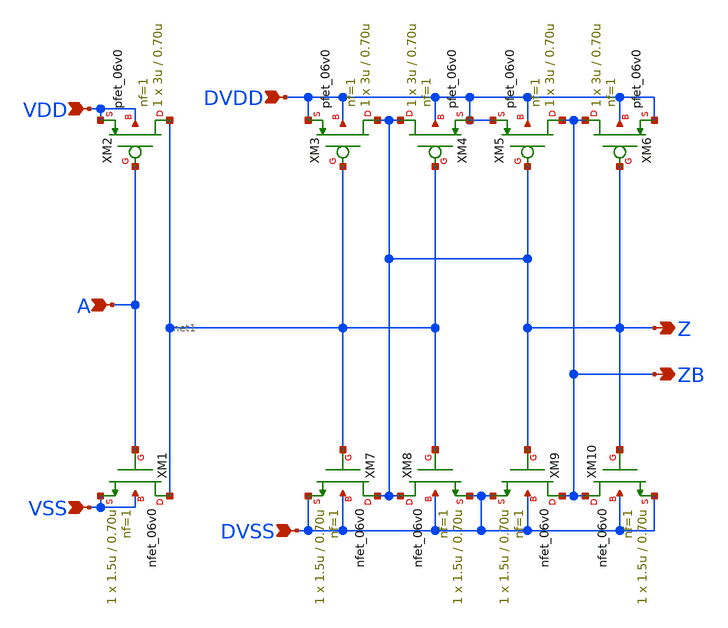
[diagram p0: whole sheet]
** sch_path: gf180mcu_fd_io__bi_24t/comp018green_sigbuf_1.sch
**.subckt comp018green_sigbuf_1 A VDD VSS DVDD DVSS Z ZB
*.ipin A
*.ipin VDD
*.ipin VSS
*.ipin DVDD
*.ipin DVSS
*.opin Z
*.opin ZB
XM1 net1 A VSS VSS nfet_06v0 L=0.70u W=1.5u nf=1 ad='int((nf+1)/2) * W/nf * 0.18u' as='int((nf+2)/2) * W/nf * 0.18u'
+ pd='2*int((nf+1)/2) * (W/nf + 0.18u)' ps='2*int((nf+2)/2) * (W/nf + 0.18u)' nrd='0.18u / W' nrs='0.18u / W'
+ sa=0 sb=0 sd=0 m=1
XM2 net1 A VDD VDD pfet_06v0 L=0.70u W=3u nf=1 ad='int((nf+1)/2) * W/nf * 0.18u' as='int((nf+2)/2) * W/nf * 0.18u'
+ pd='2*int((nf+1)/2) * (W/nf + 0.18u)' ps='2*int((nf+2)/2) * (W/nf + 0.18u)' nrd='0.18u / W' nrs='0.18u / W'
+ sa=0 sb=0 sd=0 m=1
XM3 Z net1 DVDD DVDD pfet_06v0 L=0.70u W=3u nf=1 ad='int((nf+1)/2) * W/nf * 0.18u' as='int((nf+2)/2) * W/nf * 0.18u'
+ pd='2*int((nf+1)/2) * (W/nf + 0.18u)' ps='2*int((nf+2)/2) * (W/nf + 0.18u)' nrd='0.18u / W' nrs='0.18u / W'
+ sa=0 sb=0 sd=0 m=1
XM4 Z net1 DVDD DVDD pfet_06v0 L=0.70u W=3u nf=1 ad='int((nf+1)/2) * W/nf * 0.18u' as='int((nf+2)/2) * W/nf * 0.18u'
+ pd='2*int((nf+1)/2) * (W/nf + 0.18u)' ps='2*int((nf+2)/2) * (W/nf + 0.18u)' nrd='0.18u / W' nrs='0.18u / W'
+ sa=0 sb=0 sd=0 m=1
XM5 ZB Z DVDD DVDD pfet_06v0 L=0.70u W=3u nf=1 ad='int((nf+1)/2) * W/nf * 0.18u' as='int((nf+2)/2) * W/nf * 0.18u'
+ pd='2*int((nf+1)/2) * (W/nf + 0.18u)' ps='2*int((nf+2)/2) * (W/nf + 0.18u)' nrd='0.18u / W' nrs='0.18u / W'
+ sa=0 sb=0 sd=0 m=1
XM6 ZB Z DVDD DVDD pfet_06v0 L=0.70u W=3u nf=1 ad='int((nf+1)/2) * W/nf * 0.18u' as='int((nf+2)/2) * W/nf * 0.18u'
+ pd='2*int((nf+1)/2) * (W/nf + 0.18u)' ps='2*int((nf+2)/2) * (W/nf + 0.18u)' nrd='0.18u / W' nrs='0.18u / W'
+ sa=0 sb=0 sd=0 m=1
XM7 Z net1 DVSS DVSS nfet_06v0 L=0.70u W=1.5u nf=1 ad='int((nf+1)/2) * W/nf * 0.18u' as='int((nf+2)/2) * W/nf * 0.18u'
+ pd='2*int((nf+1)/2) * (W/nf + 0.18u)' ps='2*int((nf+2)/2) * (W/nf + 0.18u)' nrd='0.18u / W' nrs='0.18u / W'
+ sa=0 sb=0 sd=0 m=1
XM8 Z net1 DVSS DVSS nfet_06v0 L=0.70u W=1.5u nf=1 ad='int((nf+1)/2) * W/nf * 0.18u' as='int((nf+2)/2) * W/nf * 0.18u'
+ pd='2*int((nf+1)/2) * (W/nf + 0.18u)' ps='2*int((nf+2)/2) * (W/nf + 0.18u)' nrd='0.18u / W' nrs='0.18u / W'
+ sa=0 sb=0 sd=0 m=1
XM9 ZB Z DVSS DVSS nfet_06v0 L=0.70u W=1.5u nf=1 ad='int((nf+1)/2) * W/nf * 0.18u' as='int((nf+2)/2) * W/nf * 0.18u'
+ pd='2*int((nf+1)/2) * (W/nf + 0.18u)' ps='2*int((nf+2)/2) * (W/nf + 0.18u)' nrd='0.18u / W' nrs='0.18u / W'
+ sa=0 sb=0 sd=0 m=1
XM10 ZB Z DVSS DVSS nfet_06v0 L=0.70u W=1.5u nf=1 ad='int((nf+1)/2) * W/nf * 0.18u' as='int((nf+2)/2) * W/nf * 0.18u'
+ pd='2*int((nf+1)/2) * (W/nf + 0.18u)' ps='2*int((nf+2)/2) * (W/nf + 0.18u)' nrd='0.18u / W' nrs='0.18u / W'
+ sa=0 sb=0 sd=0 m=1
**.ends
.end
